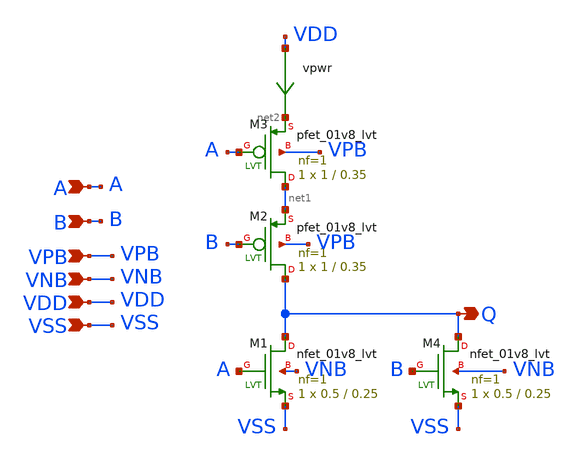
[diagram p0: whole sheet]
** sch_path: xschem/pll_nor.sch
**.subckt pll_nor Q A B VDD VPB VNB VSS
*.opin Q
*.ipin A
*.ipin B
*.ipin VDD
*.ipin VPB
*.ipin VNB
*.ipin VSS
XM3 net1 A net2 VPB sky130_fd_pr__pfet_01v8_lvt L=0.35 W=1 nf=1 ad='int((nf+1)/2) * W/nf * 0.29' as='int((nf+2)/2) * W/nf * 0.29'
+ pd='2*int((nf+1)/2) * (W/nf + 0.29)' ps='2*int((nf+2)/2) * (W/nf + 0.29)' nrd='0.29 / W' nrs='0.29 / W'
+ sa=0 sb=0 sd=0 mult=1 m=1
vpwr VDD net2 0
.save i(vpwr)
XM1 Q A VSS VNB sky130_fd_pr__nfet_01v8_lvt L=0.25 W=0.5 nf=1 ad='int((nf+1)/2) * W/nf * 0.29' as='int((nf+2)/2) * W/nf * 0.29'
+ pd='2*int((nf+1)/2) * (W/nf + 0.29)' ps='2*int((nf+2)/2) * (W/nf + 0.29)' nrd='0.29 / W' nrs='0.29 / W'
+ sa=0 sb=0 sd=0 mult=1 m=1
XM2 Q B net1 VPB sky130_fd_pr__pfet_01v8_lvt L=0.35 W=1 nf=1 ad='int((nf+1)/2) * W/nf * 0.29' as='int((nf+2)/2) * W/nf * 0.29'
+ pd='2*int((nf+1)/2) * (W/nf + 0.29)' ps='2*int((nf+2)/2) * (W/nf + 0.29)' nrd='0.29 / W' nrs='0.29 / W'
+ sa=0 sb=0 sd=0 mult=1 m=1
XM4 Q B VSS VNB sky130_fd_pr__nfet_01v8_lvt L=0.25 W=0.5 nf=1 ad='int((nf+1)/2) * W/nf * 0.29' as='int((nf+2)/2) * W/nf * 0.29'
+ pd='2*int((nf+1)/2) * (W/nf + 0.29)' ps='2*int((nf+2)/2) * (W/nf + 0.29)' nrd='0.29 / W' nrs='0.29 / W'
+ sa=0 sb=0 sd=0 mult=1 m=1
**.ends
.end
